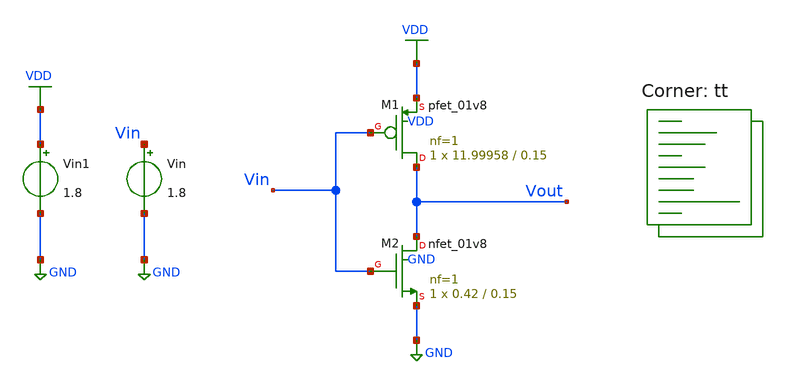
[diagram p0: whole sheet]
** sch_path: assignments/assignment2/assign1c.sch
**.subckt assign1c
Vin Vin GND 1.8
XM1 Vout Vin VDD VDD sky130_fd_pr__pfet_01v8 L=0.15 W=11.99958 nf=1 ad='int((nf+1)/2) * W/nf * 0.29'
+ as='int((nf+2)/2) * W/nf * 0.29' pd='2*int((nf+1)/2) * (W/nf + 0.29)' ps='2*int((nf+2)/2) * (W/nf + 0.29)'
+ nrd='0.29 / W' nrs='0.29 / W' sa=0 sb=0 sd=0 mult=1 m=1
XM2 Vout Vin GND GND sky130_fd_pr__nfet_01v8 L=0.15 W=0.42 nf=1 ad='int((nf+1)/2) * W/nf * 0.29' as='int((nf+2)/2) * W/nf * 0.29'
+ pd='2*int((nf+1)/2) * (W/nf + 0.29)' ps='2*int((nf+2)/2) * (W/nf + 0.29)' nrd='0.29 / W' nrs='0.29 / W'
+ sa=0 sb=0 sd=0 mult=1 m=1
Vin1 VDD GND 1.8
**** begin user architecture code


.control
let vds = 0.2
let index = 1
let N = 10
let imax = vector(N)
let vdscache = vector(N)

while index le N
	alter Vin1 $&vds
	dc Vin 0 $&vds 0.01

	let imax[index - 1] = abs(vecmin(dc{$&index}.i(Vin1)))
	let vdscache[index - 1] = vds
	print vds abs(vecmin(dc{$&index}.i(Vin1)))
	let vds = vds + 0.2
	let index = index + 1
end

* Plot all VTC curves together (now they will correctly scale from 0.2V up to 1.8V!)
plot dc1.v(Vout) dc2.v(Vout) dc3.v(Vout) dc4.v(Vout) dc5.v(Vout) dc6.v(Vout) dc7.v(Vout) dc8.v(Vout)
+ dc9.v(Vout) dc10.v(Vout)

* Plot all IDS curves together
plot dc1.i(Vin1) dc2.i(Vin1) dc3.i(Vin1) dc4.i(Vin1) dc5.i(Vin1) dc6.i(Vin1) dc7.i(Vin1) dc8.i(Vin1)
+ dc9.i(Vin1) dc10.i(Vin1)
.endc


.lib $::SKYWATER_MODELS/sky130.lib.spice tt
**** end user architecture code
**.ends
.GLOBAL GND
.GLOBAL VDD
.end
